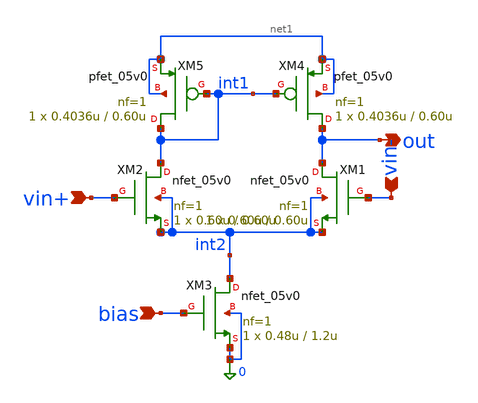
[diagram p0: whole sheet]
** sch_path: schema_ram/ota_gds.sch
**.subckt ota_gds vin+ vin- out bias
*.ipin vin+
*.ipin vin-
*.opin out
*.ipin bias
XM1 out vin- int2 int2 nfet_05v0 L=0.60u W=0.60u nf=1 ad='int((nf+1)/2) * W/nf * 0.18u' as='int((nf+2)/2) * W/nf * 0.18u'
+ pd='2*int((nf+1)/2) * (W/nf + 0.18u)' ps='2*int((nf+2)/2) * (W/nf + 0.18u)' nrd='0.18u / W' nrs='0.18u / W'
+ sa=0 sb=0 sd=0 m=1
XM3 int2 bias 0 0 nfet_05v0 L=1.2u W=0.48u nf=1 ad='int((nf+1)/2) * W/nf * 0.18u' as='int((nf+2)/2) * W/nf * 0.18u'
+ pd='2*int((nf+1)/2) * (W/nf + 0.18u)' ps='2*int((nf+2)/2) * (W/nf + 0.18u)' nrd='0.18u / W' nrs='0.18u / W'
+ sa=0 sb=0 sd=0 m=1
XM4 out int1 net1 net1 pfet_05v0 L=0.60u W=0.4036u nf=1 ad='int((nf+1)/2) * W/nf * 0.18u' as='int((nf+2)/2) * W/nf * 0.18u'
+ pd='2*int((nf+1)/2) * (W/nf + 0.18u)' ps='2*int((nf+2)/2) * (W/nf + 0.18u)' nrd='0.18u / W' nrs='0.18u / W'
+ sa=0 sb=0 sd=0 m=1
XM5 int1 int1 net1 net1 pfet_05v0 L=0.60u W=0.4036u nf=1 ad='int((nf+1)/2) * W/nf * 0.18u' as='int((nf+2)/2) * W/nf * 0.18u'
+ pd='2*int((nf+1)/2) * (W/nf + 0.18u)' ps='2*int((nf+2)/2) * (W/nf + 0.18u)' nrd='0.18u / W' nrs='0.18u / W'
+ sa=0 sb=0 sd=0 m=1
XM2 int1 vin+ int2 int2 nfet_05v0 L=0.60u W=0.60u nf=1 ad='int((nf+1)/2) * W/nf * 0.18u' as='int((nf+2)/2) * W/nf * 0.18u'
+ pd='2*int((nf+1)/2) * (W/nf + 0.18u)' ps='2*int((nf+2)/2) * (W/nf + 0.18u)' nrd='0.18u / W' nrs='0.18u / W'
+ sa=0 sb=0 sd=0 m=1
**.ends
.end
